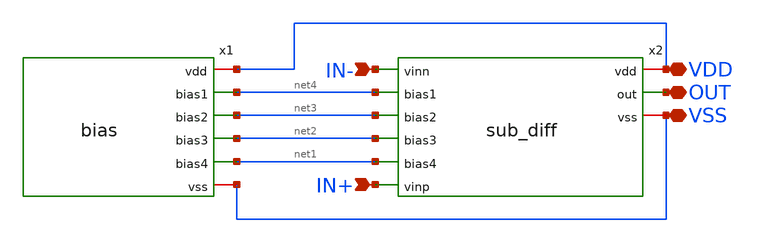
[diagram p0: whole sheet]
** sch_path: FINAL/XSCHEM/OPAM/COMP_sc.sch
**.subckt COMP_sc IN- IN+ VDD VSS OUT
*.ipin IN-
*.ipin IN+
*.iopin VDD
*.iopin VSS
*.iopin OUT
x1 VDD net4 net3 net2 net1 VSS bias
x2 VDD net4 net3 IN- OUT IN+ net2 net1 VSS sub_diff
**.ends
.end
